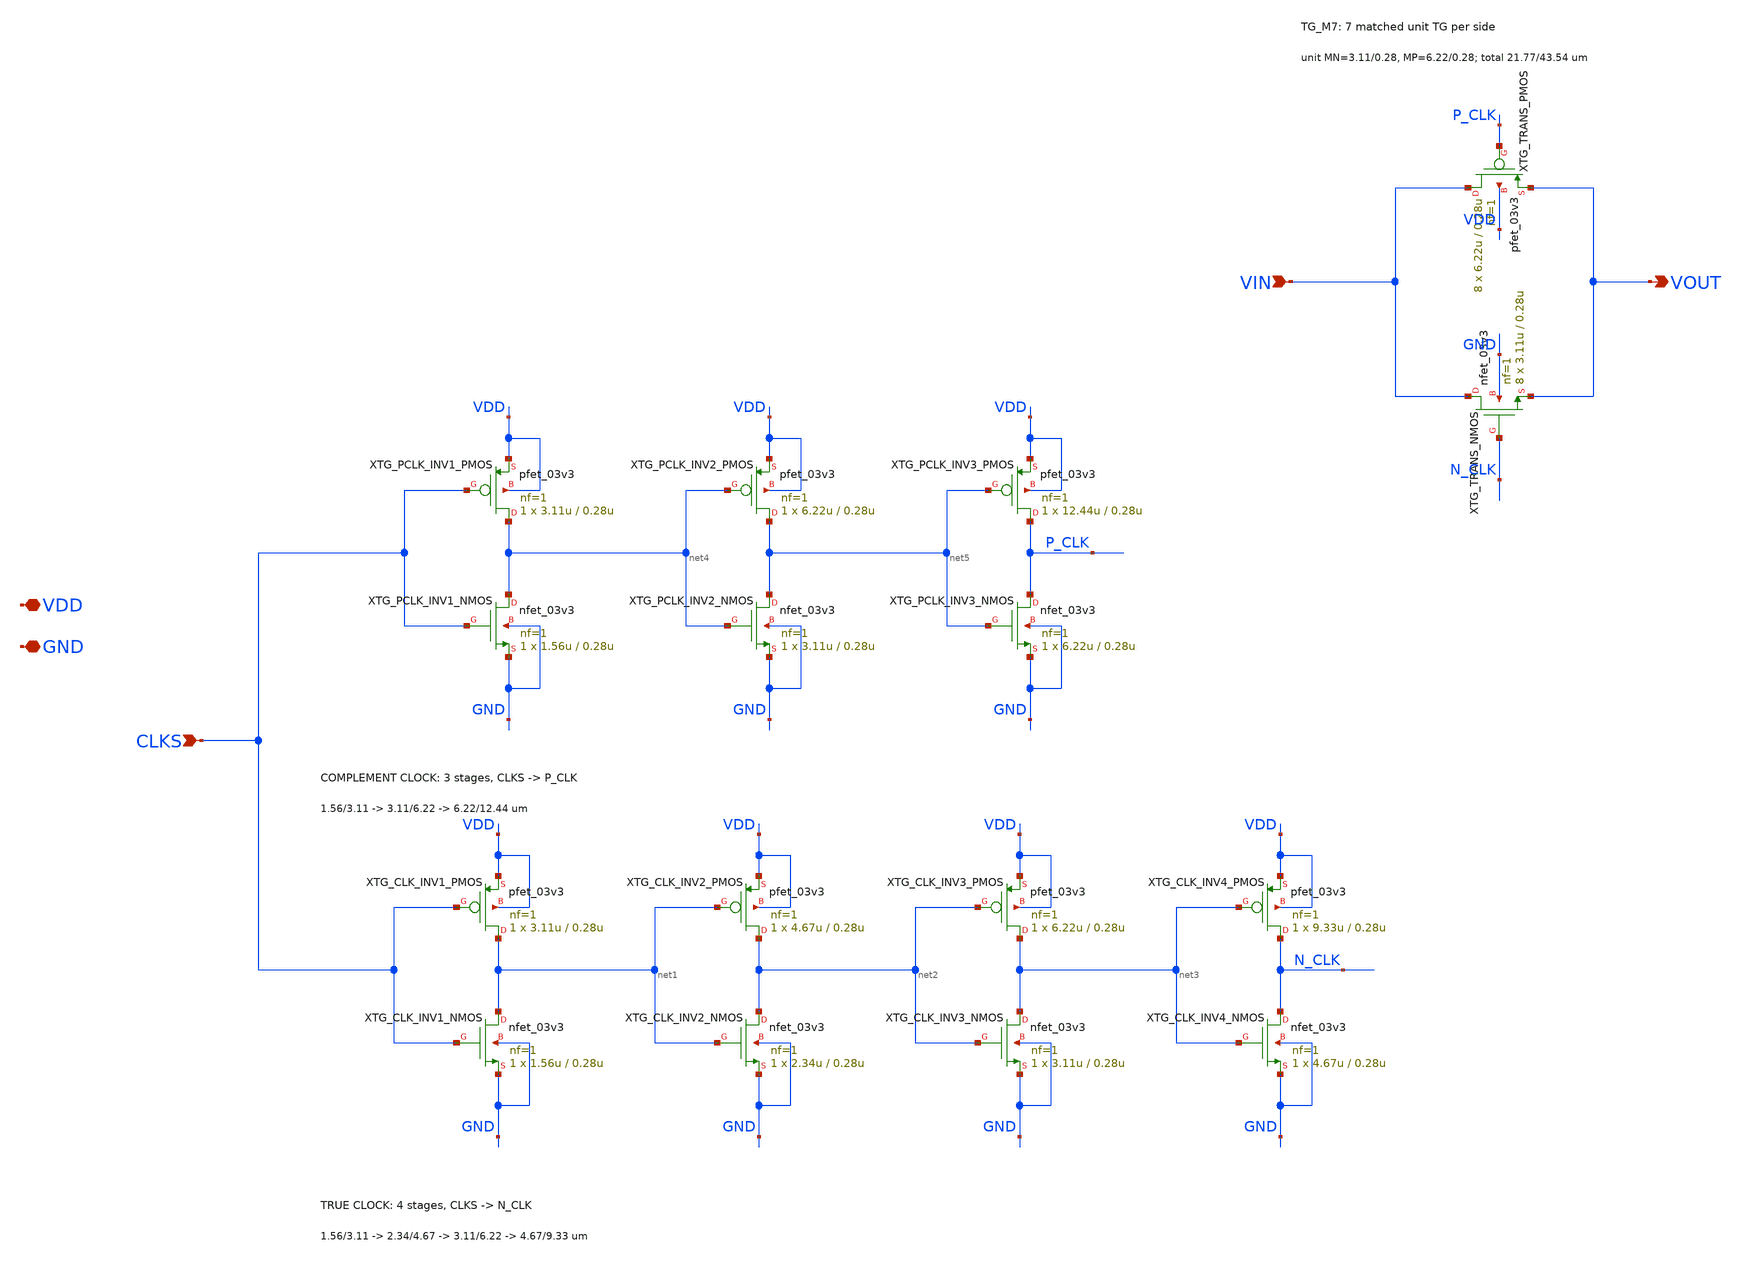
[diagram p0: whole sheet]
** sch_path: verification/a44_w5p29_trans_driver/01_CURRENT_CIRCUIT_FILES/xschem/A44_SWITCH_TRANS_TG8.sch
**.subckt A44_SWITCH_TRANS_TG8 VDD GND VIN CLKS VOUT
*.iopin VDD
*.iopin GND
*.ipin VIN
*.ipin CLKS
*.opin VOUT
XTG_CLK_INV1_NMOS net1 CLKS GND GND nfet_03v3 L=0.28u W=1.56u nf=1 ad='int((nf+1)/2) * W/nf * 0.18u'
+ as='int((nf+2)/2) * W/nf * 0.18u' pd='2*int((nf+1)/2) * (W/nf + 0.18u)' ps='2*int((nf+2)/2) * (W/nf + 0.18u)'
+ nrd='0.18u / W' nrs='0.18u / W' sa=0 sb=0 sd=0 m=1
XTG_CLK_INV1_PMOS net1 CLKS VDD VDD pfet_03v3 L=0.28u W=3.11u nf=1 ad='int((nf+1)/2) * W/nf * 0.18u'
+ as='int((nf+2)/2) * W/nf * 0.18u' pd='2*int((nf+1)/2) * (W/nf + 0.18u)' ps='2*int((nf+2)/2) * (W/nf + 0.18u)'
+ nrd='0.18u / W' nrs='0.18u / W' sa=0 sb=0 sd=0 m=1
XTG_CLK_INV2_NMOS net2 net1 GND GND nfet_03v3 L=0.28u W=2.34u nf=1 ad='int((nf+1)/2) * W/nf * 0.18u'
+ as='int((nf+2)/2) * W/nf * 0.18u' pd='2*int((nf+1)/2) * (W/nf + 0.18u)' ps='2*int((nf+2)/2) * (W/nf + 0.18u)'
+ nrd='0.18u / W' nrs='0.18u / W' sa=0 sb=0 sd=0 m=1
XTG_CLK_INV2_PMOS net2 net1 VDD VDD pfet_03v3 L=0.28u W=4.67u nf=1 ad='int((nf+1)/2) * W/nf * 0.18u'
+ as='int((nf+2)/2) * W/nf * 0.18u' pd='2*int((nf+1)/2) * (W/nf + 0.18u)' ps='2*int((nf+2)/2) * (W/nf + 0.18u)'
+ nrd='0.18u / W' nrs='0.18u / W' sa=0 sb=0 sd=0 m=1
XTG_CLK_INV3_NMOS net3 net2 GND GND nfet_03v3 L=0.28u W=3.11u nf=1 ad='int((nf+1)/2) * W/nf * 0.18u'
+ as='int((nf+2)/2) * W/nf * 0.18u' pd='2*int((nf+1)/2) * (W/nf + 0.18u)' ps='2*int((nf+2)/2) * (W/nf + 0.18u)'
+ nrd='0.18u / W' nrs='0.18u / W' sa=0 sb=0 sd=0 m=1
XTG_CLK_INV3_PMOS net3 net2 VDD VDD pfet_03v3 L=0.28u W=6.22u nf=1 ad='int((nf+1)/2) * W/nf * 0.18u'
+ as='int((nf+2)/2) * W/nf * 0.18u' pd='2*int((nf+1)/2) * (W/nf + 0.18u)' ps='2*int((nf+2)/2) * (W/nf + 0.18u)'
+ nrd='0.18u / W' nrs='0.18u / W' sa=0 sb=0 sd=0 m=1
XTG_CLK_INV4_NMOS N_CLK net3 GND GND nfet_03v3 L=0.28u W=4.67u nf=1 ad='int((nf+1)/2) * W/nf * 0.18u'
+ as='int((nf+2)/2) * W/nf * 0.18u' pd='2*int((nf+1)/2) * (W/nf + 0.18u)' ps='2*int((nf+2)/2) * (W/nf + 0.18u)'
+ nrd='0.18u / W' nrs='0.18u / W' sa=0 sb=0 sd=0 m=1
XTG_CLK_INV4_PMOS N_CLK net3 VDD VDD pfet_03v3 L=0.28u W=9.33u nf=1 ad='int((nf+1)/2) * W/nf * 0.18u'
+ as='int((nf+2)/2) * W/nf * 0.18u' pd='2*int((nf+1)/2) * (W/nf + 0.18u)' ps='2*int((nf+2)/2) * (W/nf + 0.18u)'
+ nrd='0.18u / W' nrs='0.18u / W' sa=0 sb=0 sd=0 m=1
XTG_PCLK_INV1_NMOS net4 CLKS GND GND nfet_03v3 L=0.28u W=1.56u nf=1 ad='int((nf+1)/2) * W/nf * 0.18u'
+ as='int((nf+2)/2) * W/nf * 0.18u' pd='2*int((nf+1)/2) * (W/nf + 0.18u)' ps='2*int((nf+2)/2) * (W/nf + 0.18u)'
+ nrd='0.18u / W' nrs='0.18u / W' sa=0 sb=0 sd=0 m=1
XTG_PCLK_INV1_PMOS net4 CLKS VDD VDD pfet_03v3 L=0.28u W=3.11u nf=1 ad='int((nf+1)/2) * W/nf * 0.18u'
+ as='int((nf+2)/2) * W/nf * 0.18u' pd='2*int((nf+1)/2) * (W/nf + 0.18u)' ps='2*int((nf+2)/2) * (W/nf + 0.18u)'
+ nrd='0.18u / W' nrs='0.18u / W' sa=0 sb=0 sd=0 m=1
XTG_PCLK_INV2_NMOS net5 net4 GND GND nfet_03v3 L=0.28u W=3.11u nf=1 ad='int((nf+1)/2) * W/nf * 0.18u'
+ as='int((nf+2)/2) * W/nf * 0.18u' pd='2*int((nf+1)/2) * (W/nf + 0.18u)' ps='2*int((nf+2)/2) * (W/nf + 0.18u)'
+ nrd='0.18u / W' nrs='0.18u / W' sa=0 sb=0 sd=0 m=1
XTG_PCLK_INV2_PMOS net5 net4 VDD VDD pfet_03v3 L=0.28u W=6.22u nf=1 ad='int((nf+1)/2) * W/nf * 0.18u'
+ as='int((nf+2)/2) * W/nf * 0.18u' pd='2*int((nf+1)/2) * (W/nf + 0.18u)' ps='2*int((nf+2)/2) * (W/nf + 0.18u)'
+ nrd='0.18u / W' nrs='0.18u / W' sa=0 sb=0 sd=0 m=1
XTG_PCLK_INV3_NMOS P_CLK net5 GND GND nfet_03v3 L=0.28u W=6.22u nf=1 ad='int((nf+1)/2) * W/nf * 0.18u'
+ as='int((nf+2)/2) * W/nf * 0.18u' pd='2*int((nf+1)/2) * (W/nf + 0.18u)' ps='2*int((nf+2)/2) * (W/nf + 0.18u)'
+ nrd='0.18u / W' nrs='0.18u / W' sa=0 sb=0 sd=0 m=1
XTG_PCLK_INV3_PMOS P_CLK net5 VDD VDD pfet_03v3 L=0.28u W=12.44u nf=1 ad='int((nf+1)/2) * W/nf * 0.18u'
+ as='int((nf+2)/2) * W/nf * 0.18u' pd='2*int((nf+1)/2) * (W/nf + 0.18u)' ps='2*int((nf+2)/2) * (W/nf + 0.18u)'
+ nrd='0.18u / W' nrs='0.18u / W' sa=0 sb=0 sd=0 m=1
XTG_TRANS_NMOS VIN N_CLK VOUT GND nfet_03v3 L=0.28u W=3.11u nf=1 ad='int((nf+1)/2) * W/nf * 0.18u' as='int((nf+2)/2) * W/nf * 0.18u'
+ pd='2*int((nf+1)/2) * (W/nf + 0.18u)' ps='2*int((nf+2)/2) * (W/nf + 0.18u)' nrd='0.18u / W' nrs='0.18u / W'
+ sa=0 sb=0 sd=0 m=8
XTG_TRANS_PMOS VIN P_CLK VOUT VDD pfet_03v3 L=0.28u W=6.22u nf=1 ad='int((nf+1)/2) * W/nf * 0.18u' as='int((nf+2)/2) * W/nf * 0.18u'
+ pd='2*int((nf+1)/2) * (W/nf + 0.18u)' ps='2*int((nf+2)/2) * (W/nf + 0.18u)' nrd='0.18u / W' nrs='0.18u / W'
+ sa=0 sb=0 sd=0 m=8
**.ends
.end
